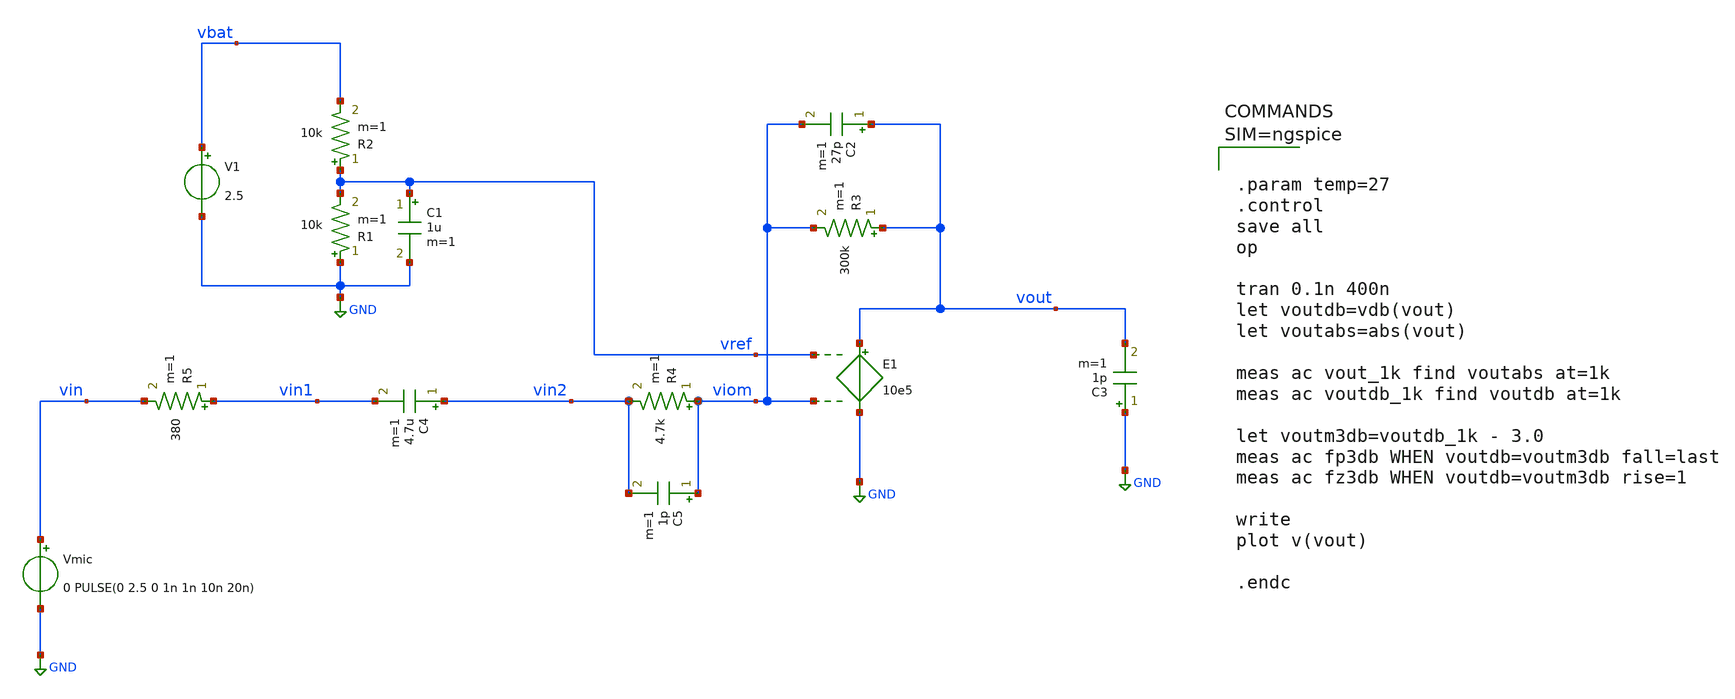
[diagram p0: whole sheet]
** sch_path: xschem/mic_transient_change5.sch
**.subckt mic_transient_change5
R1 GND vref 10k m=1
R2 vref vbat 10k m=1
C1 vref GND 1u m=1
V1 vbat GND 2.5
R3 vout viom 300k m=1
R4 viom vin2 4.7k m=1
R5 vin1 vin 380 m=1
C2 vout viom 27p m=1
E1 vout GND vref viom 10e5
C3 GND vout 1p m=1
C4 vin2 vin1 4.7u m=1
Vmic vin GND 0 PULSE(0 2.5 0 1n 1n 10n 20n)
C5 viom vin2 1p m=1
**** begin user architecture code



.param temp=27
.control
save all
op

tran 0.1n 400n
let voutdb=vdb(vout)
let voutabs=abs(vout)

meas ac vout_1k find voutabs at=1k
meas ac voutdb_1k find voutdb at=1k

let voutm3db=voutdb_1k - 3.0
meas ac fp3db WHEN voutdb=voutm3db fall=last
meas ac fz3db WHEN voutdb=voutm3db rise=1

write
plot v(vout)

.endc




**** end user architecture code
**.ends
.GLOBAL GND
.end
